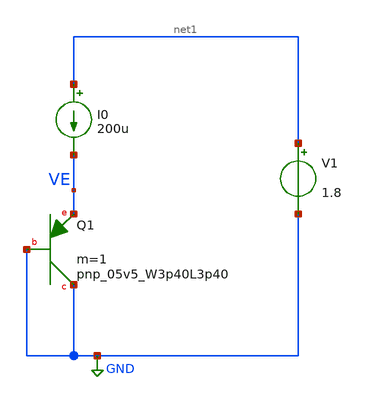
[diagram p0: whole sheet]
** sch_path: design/bgr_new/CTAT_working_bak.sch
**.subckt CTAT_working_bak
XQ1 GND GND VE sky130_fd_pr__pnp_05v5_W3p40L3p40 m=1
I0 net1 VE 200u
V1 net1 GND 1.8
**** begin user architecture code

** opencircuitdesign pdks install
.lib $::SKYWATER_MODELS/sky130.lib.spice tt_mm




.options savecurrents

*** plot vbgp with variation in supply voltage
*Vdd VDD GND 3.3
*V_en en GND 3.3
*.dc Vdd 2 4 0.1
*.control
*run
*print Vbgp
*plot V(Vbgp)
*.endc

*** plot vbgp with variation in temperature @3.3V
*Vdd VDD GND 3.3
*V_en en GND 3.3
.dc temp -40 140 1 I0 50u 500u 50u

.control
run
print V(VE)
plot V(VE)
plot deriv(V(VE))/1.202344
.endc

*** plot voltage coefficient
*Vdd VDD GND 3.3
*V_en en GND 3.3
*.dc Vdd 2 4 0.1
*.control
*run
*plot deriv(V(Vbgp))
*.endc

*** plot temperature coefficient
*Vdd VDD GND 3.3
*V_en en GND 3.3
*.dc temp -40 140 1
*.control
*run
*plot deriv(V(Vbgp))/1.202344
*.endc



*** enable pin
*Vdd VDD GND 3.3
*V_en en GND PULSE(0 3.3 0 200us 200us 600us 2000us 0)
*.tran 1u 2000us
*.control
*run
*plot V(en)
*plot -I(VDD)
*.endc


**** end user architecture code
**.ends
.GLOBAL GND
.end
